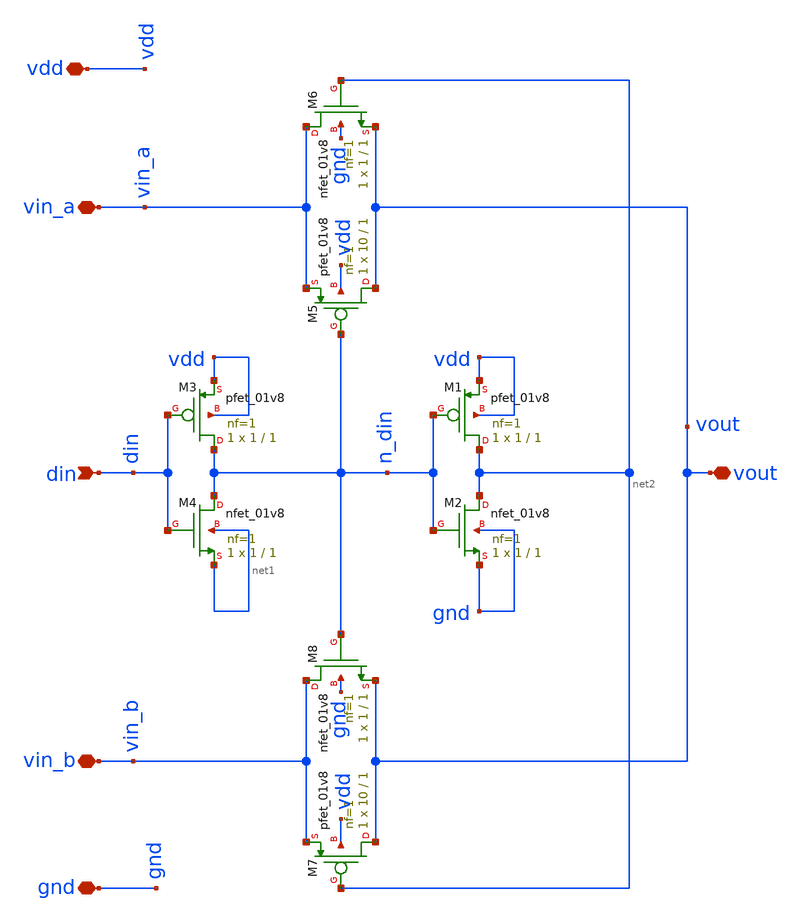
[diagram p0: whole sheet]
** sch_path: Symbols/mos_sym_spdt.sch
**.subckt mos_sym_spdt vout vin_a vin_b vdd gnd din
*.iopin vout
*.iopin vin_a
*.iopin vin_b
*.iopin vdd
*.iopin gnd
*.ipin din
XM3 n_din din vdd vdd sky130_fd_pr__pfet_01v8 L=1 W=1 nf=1 ad='int((nf+1)/2) * W/nf * 0.29' as='int((nf+2)/2) * W/nf * 0.29'
+ pd='2*int((nf+1)/2) * (W/nf + 0.29)' ps='2*int((nf+2)/2) * (W/nf + 0.29)' nrd='0.29 / W' nrs='0.29 / W'
+ sa=0 sb=0 sd=0 mult=1 m=1
XM4 n_din din net1 net1 sky130_fd_pr__nfet_01v8 L=1 W=1 nf=1 ad='int((1 + 1)/2) * 1 / 1 * 0.29' as='int((1 + 2)/2) * 1 / 1 * 0.29'
+ pd='2*int((1 + 1)/2) * (1 / 1 + 0.29)' ps='2*int((1 + 2)/2) * (1 / 1 + 0.29)' nrd='0.29 / 1 ' nrs='0.29 / 1 '
+ sa=0 sb=0 sd=0 mult=1 m=1
XM1 net2 n_din vdd vdd sky130_fd_pr__pfet_01v8 L=1 W=1 nf=1 ad='int((nf+1)/2) * W/nf * 0.29' as='int((nf+2)/2) * W/nf * 0.29'
+ pd='2*int((nf+1)/2) * (W/nf + 0.29)' ps='2*int((nf+2)/2) * (W/nf + 0.29)' nrd='0.29 / W' nrs='0.29 / W'
+ sa=0 sb=0 sd=0 mult=1 m=1
XM2 net2 n_din gnd gnd sky130_fd_pr__nfet_01v8 L=1 W=1 nf=1 ad='int((1 + 1)/2) * 1 / 1 * 0.29' as='int((1 + 2)/2) * 1 / 1 * 0.29'
+ pd='2*int((1 + 1)/2) * (1 / 1 + 0.29)' ps='2*int((1 + 2)/2) * (1 / 1 + 0.29)' nrd='0.29 / 1 ' nrs='0.29 / 1 '
+ sa=0 sb=0 sd=0 mult=1 m=1
XM5 vout n_din vin_a vdd sky130_fd_pr__pfet_01v8 L=1 W=10 nf=1 ad='int((nf+1)/2) * W/nf * 0.29' as='int((nf+2)/2) * W/nf * 0.29'
+ pd='2*int((nf+1)/2) * (W/nf + 0.29)' ps='2*int((nf+2)/2) * (W/nf + 0.29)' nrd='0.29 / W' nrs='0.29 / W'
+ sa=0 sb=0 sd=0 mult=1 m=1
XM6 vin_a net2 vout gnd sky130_fd_pr__nfet_01v8 L=1 W=1 nf=1 ad='int((1 + 1)/2) * 1 / 1 * 0.29' as='int((1 + 2)/2) * 1 / 1 * 0.29'
+ pd='2*int((1 + 1)/2) * (1 / 1 + 0.29)' ps='2*int((1 + 2)/2) * (1 / 1 + 0.29)' nrd='0.29 / 1 ' nrs='0.29 / 1 '
+ sa=0 sb=0 sd=0 mult=1 m=1
XM7 vout net2 vin_b vdd sky130_fd_pr__pfet_01v8 L=1 W=10 nf=1 ad='int((nf+1)/2) * W/nf * 0.29' as='int((nf+2)/2) * W/nf * 0.29'
+ pd='2*int((nf+1)/2) * (W/nf + 0.29)' ps='2*int((nf+2)/2) * (W/nf + 0.29)' nrd='0.29 / W' nrs='0.29 / W'
+ sa=0 sb=0 sd=0 mult=1 m=1
XM8 vin_b n_din vout gnd sky130_fd_pr__nfet_01v8 L=1 W=1 nf=1 ad='int((1 + 1)/2) * 1 / 1 * 0.29' as='int((1 + 2)/2) * 1 / 1 * 0.29'
+ pd='2*int((1 + 1)/2) * (1 / 1 + 0.29)' ps='2*int((1 + 2)/2) * (1 / 1 + 0.29)' nrd='0.29 / 1 ' nrs='0.29 / 1 '
+ sa=0 sb=0 sd=0 mult=1 m=1
**.ends
.end
